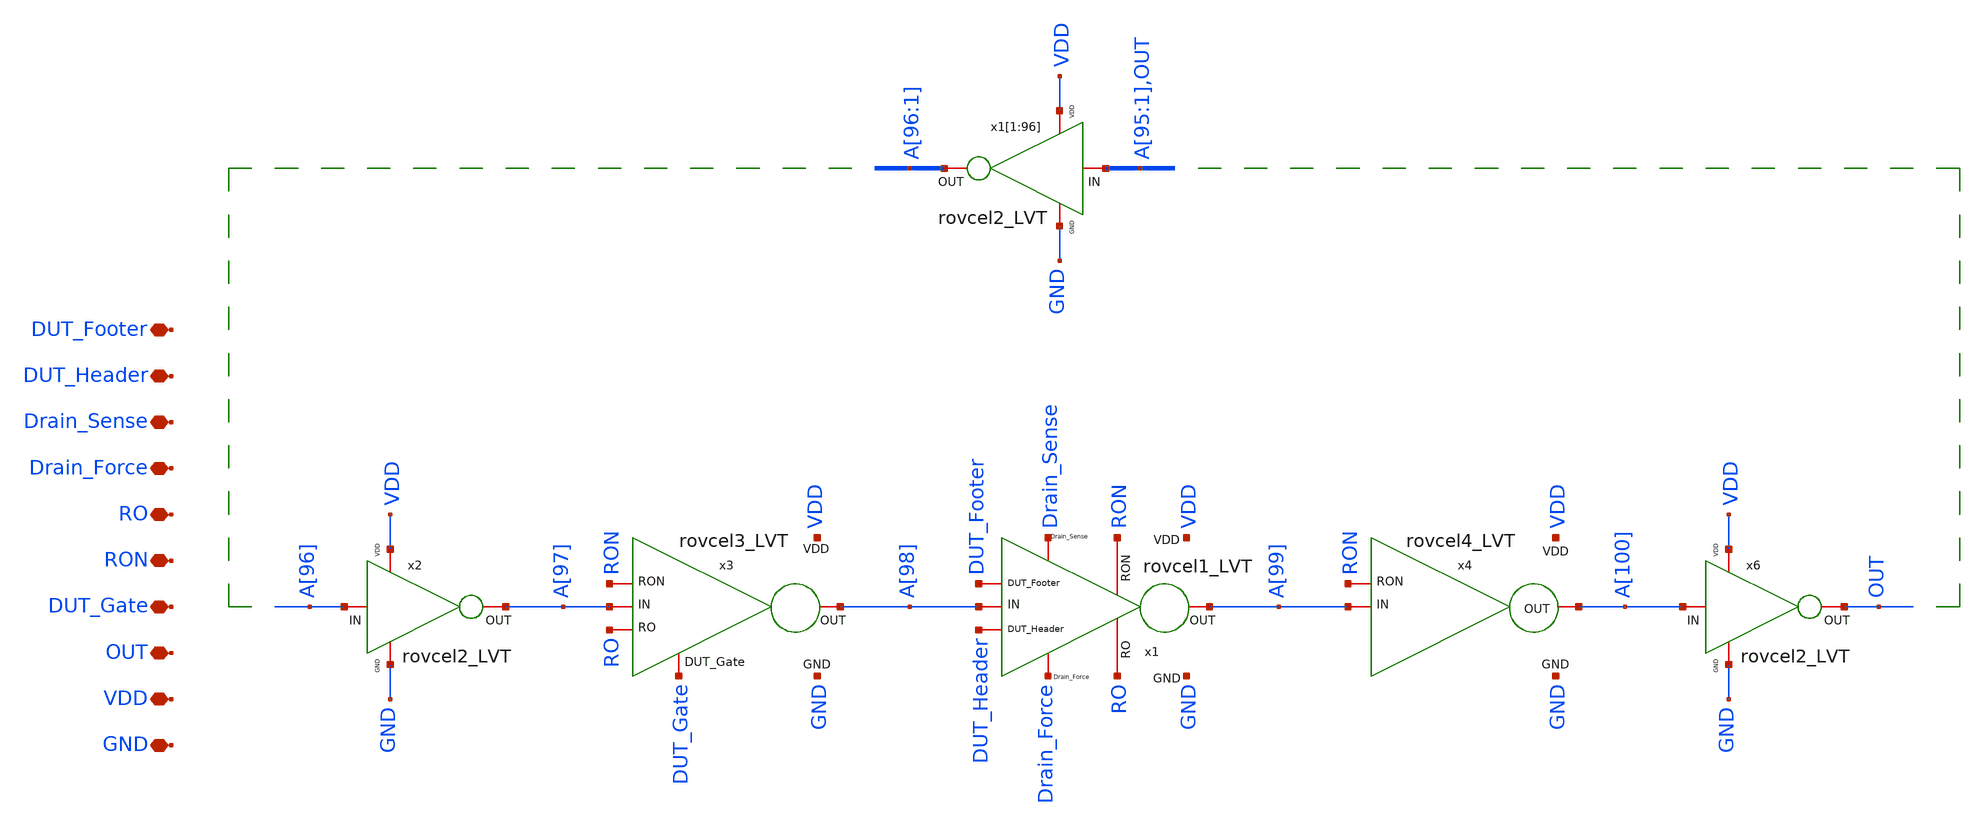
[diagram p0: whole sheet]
** sch_path: LVT/RO_LVT_101St/RO_LVT_101St.sch
**.subckt RO_LVT_101St DUT_Footer DUT_Header Drain_Sense Drain_Force RON RO DUT_Gate OUT GND VDD
*.iopin DUT_Footer
*.iopin DUT_Header
*.iopin Drain_Sense
*.iopin Drain_Force
*.iopin RON
*.iopin RO
*.iopin DUT_Gate
*.iopin OUT
*.iopin GND
*.iopin VDD
x2 VDD GND A[96] A[97] rovcel2_LVT
x6 VDD GND A[100] OUT rovcel2_LVT
x1[1] VDD GND A[95] A[96] rovcel2_LVT
x1[2] VDD GND A[94] A[95] rovcel2_LVT
x1[3] VDD GND A[93] A[94] rovcel2_LVT
x1[4] VDD GND A[92] A[93] rovcel2_LVT
x1[5] VDD GND A[91] A[92] rovcel2_LVT
x1[6] VDD GND A[90] A[91] rovcel2_LVT
x1[7] VDD GND A[89] A[90] rovcel2_LVT
x1[8] VDD GND A[88] A[89] rovcel2_LVT
x1[9] VDD GND A[87] A[88] rovcel2_LVT
x1[10] VDD GND A[86] A[87] rovcel2_LVT
x1[11] VDD GND A[85] A[86] rovcel2_LVT
x1[12] VDD GND A[84] A[85] rovcel2_LVT
x1[13] VDD GND A[83] A[84] rovcel2_LVT
x1[14] VDD GND A[82] A[83] rovcel2_LVT
x1[15] VDD GND A[81] A[82] rovcel2_LVT
x1[16] VDD GND A[80] A[81] rovcel2_LVT
x1[17] VDD GND A[79] A[80] rovcel2_LVT
x1[18] VDD GND A[78] A[79] rovcel2_LVT
x1[19] VDD GND A[77] A[78] rovcel2_LVT
x1[20] VDD GND A[76] A[77] rovcel2_LVT
x1[21] VDD GND A[75] A[76] rovcel2_LVT
x1[22] VDD GND A[74] A[75] rovcel2_LVT
x1[23] VDD GND A[73] A[74] rovcel2_LVT
x1[24] VDD GND A[72] A[73] rovcel2_LVT
x1[25] VDD GND A[71] A[72] rovcel2_LVT
x1[26] VDD GND A[70] A[71] rovcel2_LVT
x1[27] VDD GND A[69] A[70] rovcel2_LVT
x1[28] VDD GND A[68] A[69] rovcel2_LVT
x1[29] VDD GND A[67] A[68] rovcel2_LVT
x1[30] VDD GND A[66] A[67] rovcel2_LVT
x1[31] VDD GND A[65] A[66] rovcel2_LVT
x1[32] VDD GND A[64] A[65] rovcel2_LVT
x1[33] VDD GND A[63] A[64] rovcel2_LVT
x1[34] VDD GND A[62] A[63] rovcel2_LVT
x1[35] VDD GND A[61] A[62] rovcel2_LVT
x1[36] VDD GND A[60] A[61] rovcel2_LVT
x1[37] VDD GND A[59] A[60] rovcel2_LVT
x1[38] VDD GND A[58] A[59] rovcel2_LVT
x1[39] VDD GND A[57] A[58] rovcel2_LVT
x1[40] VDD GND A[56] A[57] rovcel2_LVT
x1[41] VDD GND A[55] A[56] rovcel2_LVT
x1[42] VDD GND A[54] A[55] rovcel2_LVT
x1[43] VDD GND A[53] A[54] rovcel2_LVT
x1[44] VDD GND A[52] A[53] rovcel2_LVT
x1[45] VDD GND A[51] A[52] rovcel2_LVT
x1[46] VDD GND A[50] A[51] rovcel2_LVT
x1[47] VDD GND A[49] A[50] rovcel2_LVT
x1[48] VDD GND A[48] A[49] rovcel2_LVT
x1[49] VDD GND A[47] A[48] rovcel2_LVT
x1[50] VDD GND A[46] A[47] rovcel2_LVT
x1[51] VDD GND A[45] A[46] rovcel2_LVT
x1[52] VDD GND A[44] A[45] rovcel2_LVT
x1[53] VDD GND A[43] A[44] rovcel2_LVT
x1[54] VDD GND A[42] A[43] rovcel2_LVT
x1[55] VDD GND A[41] A[42] rovcel2_LVT
x1[56] VDD GND A[40] A[41] rovcel2_LVT
x1[57] VDD GND A[39] A[40] rovcel2_LVT
x1[58] VDD GND A[38] A[39] rovcel2_LVT
x1[59] VDD GND A[37] A[38] rovcel2_LVT
x1[60] VDD GND A[36] A[37] rovcel2_LVT
x1[61] VDD GND A[35] A[36] rovcel2_LVT
x1[62] VDD GND A[34] A[35] rovcel2_LVT
x1[63] VDD GND A[33] A[34] rovcel2_LVT
x1[64] VDD GND A[32] A[33] rovcel2_LVT
x1[65] VDD GND A[31] A[32] rovcel2_LVT
x1[66] VDD GND A[30] A[31] rovcel2_LVT
x1[67] VDD GND A[29] A[30] rovcel2_LVT
x1[68] VDD GND A[28] A[29] rovcel2_LVT
x1[69] VDD GND A[27] A[28] rovcel2_LVT
x1[70] VDD GND A[26] A[27] rovcel2_LVT
x1[71] VDD GND A[25] A[26] rovcel2_LVT
x1[72] VDD GND A[24] A[25] rovcel2_LVT
x1[73] VDD GND A[23] A[24] rovcel2_LVT
x1[74] VDD GND A[22] A[23] rovcel2_LVT
x1[75] VDD GND A[21] A[22] rovcel2_LVT
x1[76] VDD GND A[20] A[21] rovcel2_LVT
x1[77] VDD GND A[19] A[20] rovcel2_LVT
x1[78] VDD GND A[18] A[19] rovcel2_LVT
x1[79] VDD GND A[17] A[18] rovcel2_LVT
x1[80] VDD GND A[16] A[17] rovcel2_LVT
x1[81] VDD GND A[15] A[16] rovcel2_LVT
x1[82] VDD GND A[14] A[15] rovcel2_LVT
x1[83] VDD GND A[13] A[14] rovcel2_LVT
x1[84] VDD GND A[12] A[13] rovcel2_LVT
x1[85] VDD GND A[11] A[12] rovcel2_LVT
x1[86] VDD GND A[10] A[11] rovcel2_LVT
x1[87] VDD GND A[9] A[10] rovcel2_LVT
x1[88] VDD GND A[8] A[9] rovcel2_LVT
x1[89] VDD GND A[7] A[8] rovcel2_LVT
x1[90] VDD GND A[6] A[7] rovcel2_LVT
x1[91] VDD GND A[5] A[6] rovcel2_LVT
x1[92] VDD GND A[4] A[5] rovcel2_LVT
x1[93] VDD GND A[3] A[4] rovcel2_LVT
x1[94] VDD GND A[2] A[3] rovcel2_LVT
x1[95] VDD GND A[1] A[2] rovcel2_LVT
x1[96] VDD GND OUT A[1] rovcel2_LVT
x1 VDD GND Drain_Sense DUT_Footer DUT_Header Drain_Force A[98] A[99] RON RO rovcel1_LVT
x3 VDD GND RON A[97] A[98] RO DUT_Gate rovcel3_LVT
x4 VDD A[100] GND RON A[99] rovcel4_LVT
**.ends
.end
